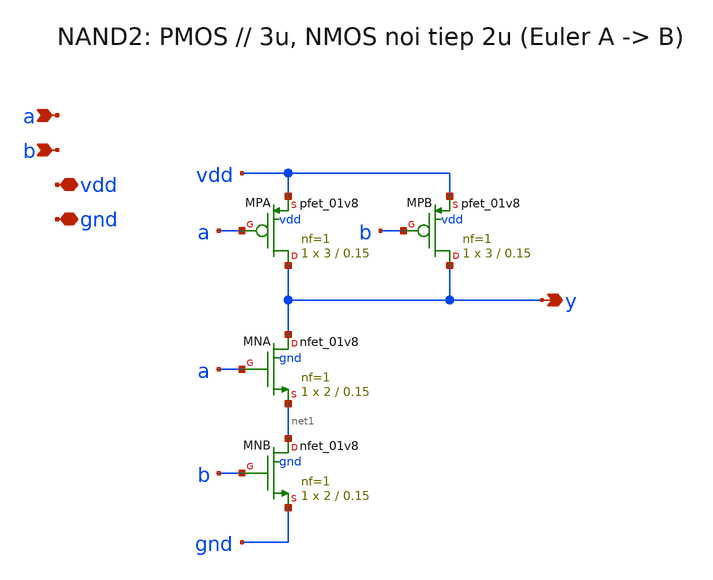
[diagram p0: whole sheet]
** sch_path: proj/xschem/nand2.sch
**.subckt nand2 a b y vdd gnd
*.ipin a
*.ipin b
*.opin y
*.iopin vdd
*.iopin gnd
XMPA y a vdd vdd sky130_fd_pr__pfet_01v8 L=0.15 W=3 nf=1 ad='int((1 + 1)/2) * 3 / 1 * 0.29' as='int((1 + 2)/2) * 3 / 1 * 0.29'
+ pd='2*int((1 + 1)/2) * (3 / 1 + 0.29)' ps='2*int((1 + 2)/2) * (3 / 1 + 0.29)' nrd='0.29 / 3 ' nrs='0.29 / 3 '
+ sa=0 sb=0 sd=0 mult=1 m=1
XMPB y b vdd vdd sky130_fd_pr__pfet_01v8 L=0.15 W=3 nf=1 ad='int((1 + 1)/2) * 3 / 1 * 0.29' as='int((1 + 2)/2) * 3 / 1 * 0.29'
+ pd='2*int((1 + 1)/2) * (3 / 1 + 0.29)' ps='2*int((1 + 2)/2) * (3 / 1 + 0.29)' nrd='0.29 / 3 ' nrs='0.29 / 3 '
+ sa=0 sb=0 sd=0 mult=1 m=1
XMNA y a net1 gnd sky130_fd_pr__nfet_01v8 L=0.15 W=2 nf=1 ad='int((nf+1)/2) * W/nf * 0.29' as='int((nf+2)/2) * W/nf * 0.29'
+ pd='2*int((nf+1)/2) * (W/nf + 0.29)' ps='2*int((nf+2)/2) * (W/nf + 0.29)' nrd='0.29 / W' nrs='0.29 / W'
+ sa=0 sb=0 sd=0 mult=1 m=1
XMNB net1 b gnd gnd sky130_fd_pr__nfet_01v8 L=0.15 W=2 nf=1 ad='int((nf+1)/2) * W/nf * 0.29' as='int((nf+2)/2) * W/nf * 0.29'
+ pd='2*int((nf+1)/2) * (W/nf + 0.29)' ps='2*int((nf+2)/2) * (W/nf + 0.29)' nrd='0.29 / W' nrs='0.29 / W'
+ sa=0 sb=0 sd=0 mult=1 m=1
**.ends
.end
